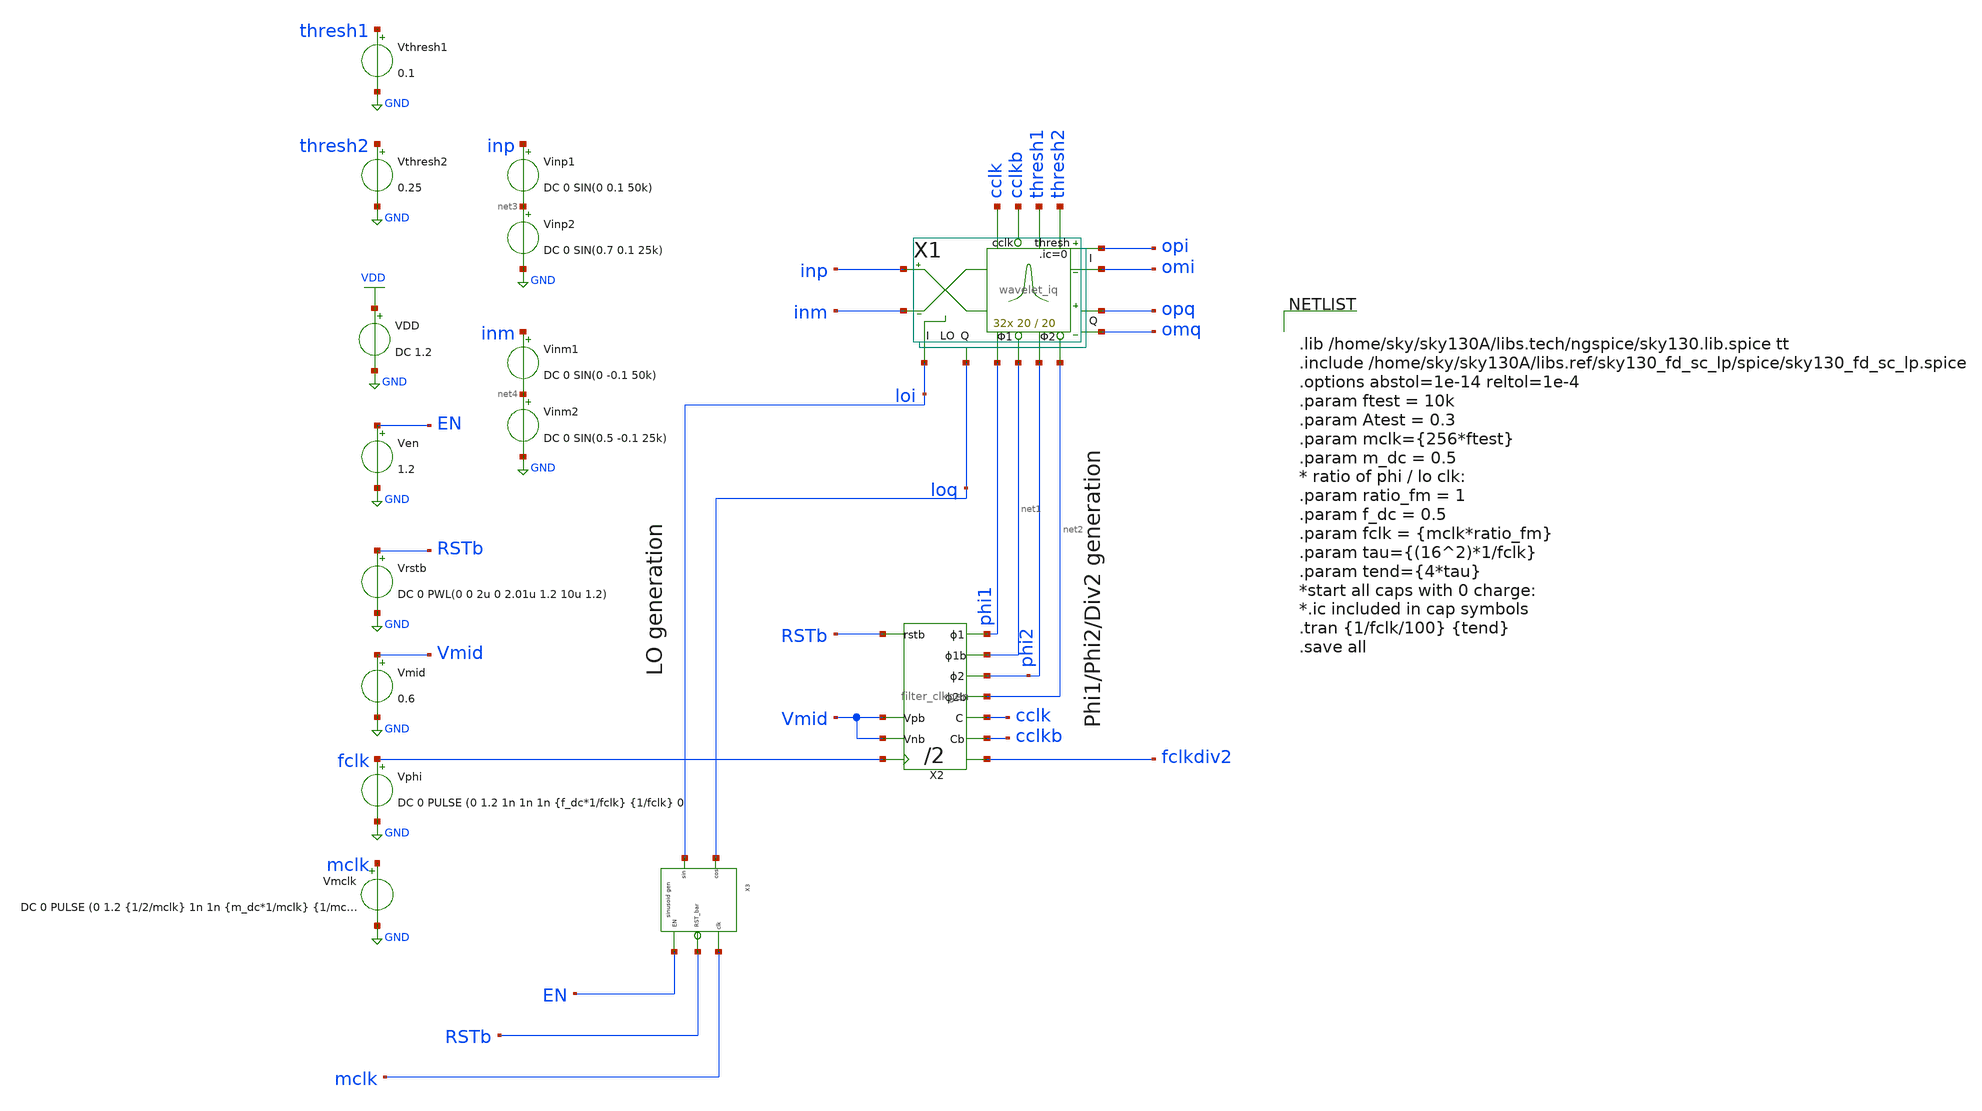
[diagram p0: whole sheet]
** sch_path: xschem/wavelet_channel/wavelet_iq_top.sch
**.subckt wavelet_iq_top
VDD VDD GND DC 1.2
Vphi fclk GND DC 0 PULSE (0 1.2 1n 1n 1n {f_dc*1/fclk} {1/fclk} 0
X1 inp opi phi1 phi2 inm omi loi loq opq omq net2 net1 cclk cclkb thresh1 thresh2 wavelet_iq W=20
+ L=20
X2 RSTb fclk net2 phi2 net1 phi1 cclkb cclk fclkdiv2 Vmid Vmid filter_clkgen
Ven EN GND 1.2
Vrstb RSTb GND DC 0 PWL(0 0 2u 0 2.01u 1.2 10u 1.2)
Vmid Vmid GND 0.6
Vmclk mclk GND DC 0 PULSE (0 1.2 {1/2/mclk} 1n 1n {m_dc*1/mclk} {1/mclk} 0
X3 EN RSTb mclk loi loq sinusoid_generator
Vthresh2 thresh2 GND 0.25
Vthresh1 thresh1 GND 0.1
Vinp1 inp net3 DC 0 SIN(0 0.1 50k)
Vinp2 net3 GND DC 0 SIN(0.7 0.1 25k)
Vinm1 inm net4 DC 0 SIN(0 -0.1 50k)
Vinm2 net4 GND DC 0 SIN(0.5 -0.1 25k)
**** begin user architecture code


.lib /home/sky/sky130A/libs.tech/ngspice/sky130.lib.spice tt
.include /home/sky/sky130A/libs.ref/sky130_fd_sc_lp/spice/sky130_fd_sc_lp.spice
.options abstol=1e-14 reltol=1e-4
.param ftest = 10k
.param Atest = 0.3
.param mclk={256*ftest}
.param m_dc = 0.5
* ratio of phi / lo clk:
.param ratio_fm = 1
.param f_dc = 0.5
.param fclk = {mclk*ratio_fm}
.param tau={(16^2)*1/fclk}
.param tend={4*tau}
*start all caps with 0 charge:
*.ic included in cap symbols
.tran {1/fclk/100} {tend}
.save all


**** end user architecture code
**.ends
.GLOBAL VDD
.GLOBAL GND
.end
